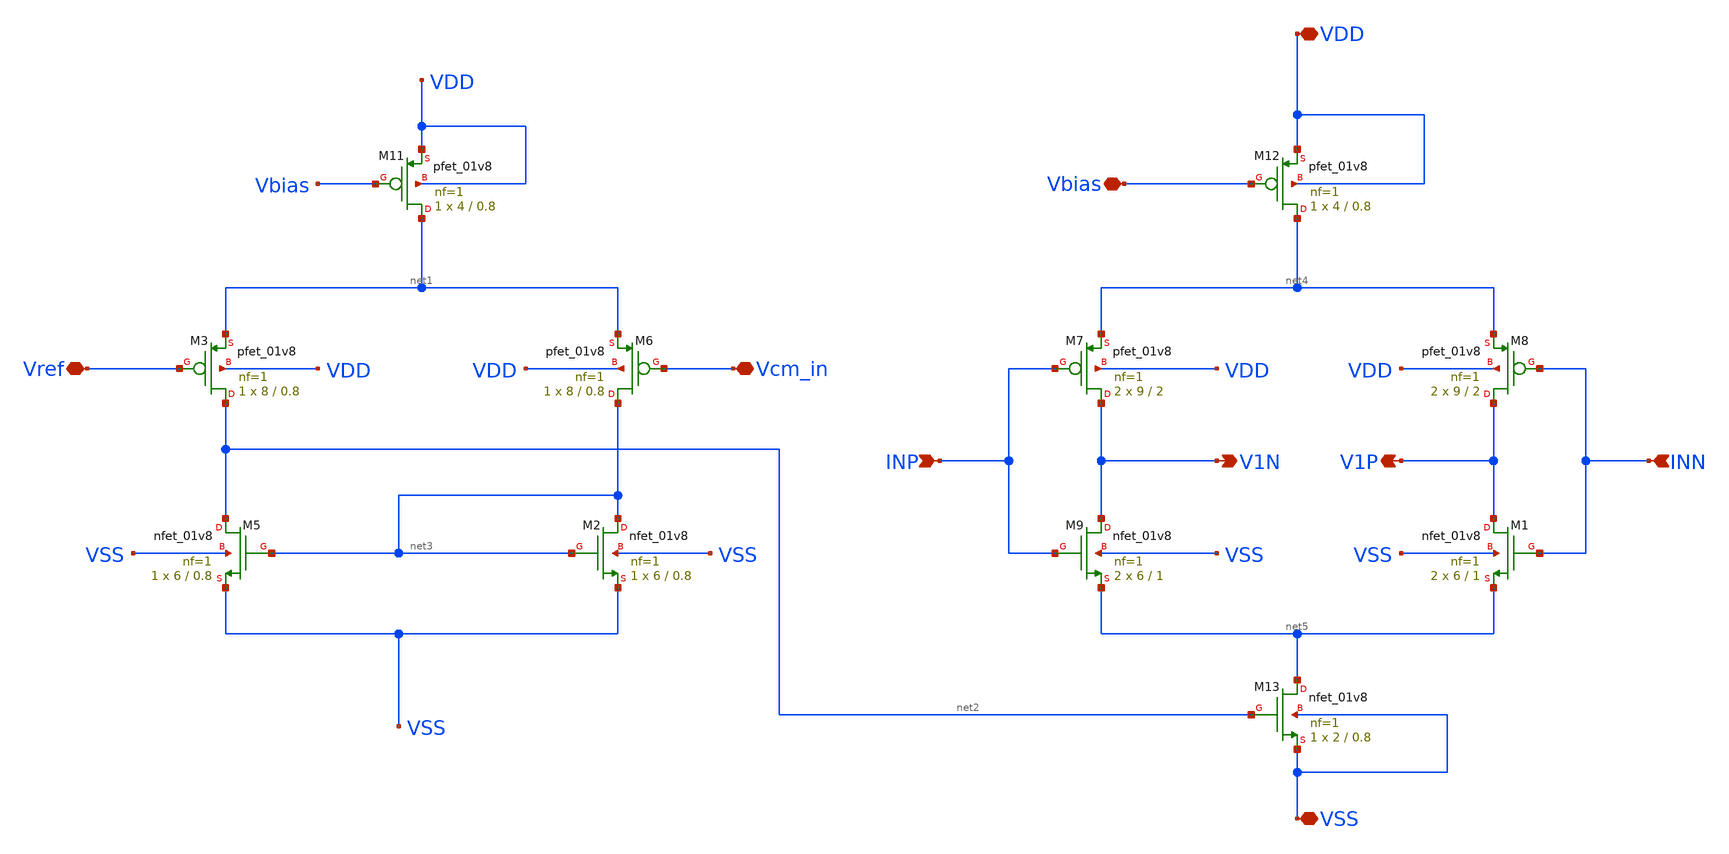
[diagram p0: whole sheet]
** sch_path: opamp_lna/low_noise_amp_simp.sch
**.subckt low_noise_amp_simp VDD VSS Vbias INP INN Vref Vcm_in V1N V1P
*.iopin VDD
*.iopin VSS
*.iopin Vbias
*.ipin INP
*.ipin INN
*.iopin Vref
*.iopin Vcm_in
*.opin V1N
*.opin V1P
XM3 net2 Vref net1 VDD sky130_fd_pr__pfet_01v8 L=0.8 W=8 nf=1 ad='int((nf+1)/2) * W/nf * 0.29' as='int((nf+2)/2) * W/nf * 0.29'
+ pd='2*int((nf+1)/2) * (W/nf + 0.29)' ps='2*int((nf+2)/2) * (W/nf + 0.29)' nrd='0.29 / W' nrs='0.29 / W'
+ sa=0 sb=0 sd=0 mult=1 m=1
XM11 net1 Vbias VDD VDD sky130_fd_pr__pfet_01v8 L=0.8 W=4 nf=1 ad='int((nf+1)/2) * W/nf * 0.29' as='int((nf+2)/2) * W/nf * 0.29'
+ pd='2*int((nf+1)/2) * (W/nf + 0.29)' ps='2*int((nf+2)/2) * (W/nf + 0.29)' nrd='0.29 / W' nrs='0.29 / W'
+ sa=0 sb=0 sd=0 mult=1 m=1
XM7 V1N INP net4 VDD sky130_fd_pr__pfet_01v8 L=2 W=9 nf=1 ad='int((nf+1)/2) * W/nf * 0.29' as='int((nf+2)/2) * W/nf * 0.29'
+ pd='2*int((nf+1)/2) * (W/nf + 0.29)' ps='2*int((nf+2)/2) * (W/nf + 0.29)' nrd='0.29 / W' nrs='0.29 / W'
+ sa=0 sb=0 sd=0 mult=2 m=2
XM8 V1P INN net4 VDD sky130_fd_pr__pfet_01v8 L=2 W=9 nf=1 ad='int((nf+1)/2) * W/nf * 0.29' as='int((nf+2)/2) * W/nf * 0.29'
+ pd='2*int((nf+1)/2) * (W/nf + 0.29)' ps='2*int((nf+2)/2) * (W/nf + 0.29)' nrd='0.29 / W' nrs='0.29 / W'
+ sa=0 sb=0 sd=0 mult=2 m=2
XM9 V1N INP net5 VSS sky130_fd_pr__nfet_01v8 L=1 W=6 nf=1 ad='int((nf+1)/2) * W/nf * 0.29' as='int((nf+2)/2) * W/nf * 0.29'
+ pd='2*int((nf+1)/2) * (W/nf + 0.29)' ps='2*int((nf+2)/2) * (W/nf + 0.29)' nrd='0.29 / W' nrs='0.29 / W'
+ sa=0 sb=0 sd=0 mult=2 m=2
XM12 net4 Vbias VDD VDD sky130_fd_pr__pfet_01v8 L=0.8 W=4 nf=1 ad='int((nf+1)/2) * W/nf * 0.29' as='int((nf+2)/2) * W/nf * 0.29'
+ pd='2*int((nf+1)/2) * (W/nf + 0.29)' ps='2*int((nf+2)/2) * (W/nf + 0.29)' nrd='0.29 / W' nrs='0.29 / W'
+ sa=0 sb=0 sd=0 mult=1 m=1
XM13 net5 net2 VSS VSS sky130_fd_pr__nfet_01v8 L=0.8 W=2 nf=1 ad='int((nf+1)/2) * W/nf * 0.29' as='int((nf+2)/2) * W/nf * 0.29'
+ pd='2*int((nf+1)/2) * (W/nf + 0.29)' ps='2*int((nf+2)/2) * (W/nf + 0.29)' nrd='0.29 / W' nrs='0.29 / W'
+ sa=0 sb=0 sd=0 mult=1 m=1
XM1 V1P INN net5 VSS sky130_fd_pr__nfet_01v8 L=1 W=6 nf=1 ad='int((nf+1)/2) * W/nf * 0.29' as='int((nf+2)/2) * W/nf * 0.29'
+ pd='2*int((nf+1)/2) * (W/nf + 0.29)' ps='2*int((nf+2)/2) * (W/nf + 0.29)' nrd='0.29 / W' nrs='0.29 / W'
+ sa=0 sb=0 sd=0 mult=2 m=2
XM2 net3 net3 VSS VSS sky130_fd_pr__nfet_01v8 L=0.8 W=6 nf=1 ad='int((nf+1)/2) * W/nf * 0.29' as='int((nf+2)/2) * W/nf * 0.29'
+ pd='2*int((nf+1)/2) * (W/nf + 0.29)' ps='2*int((nf+2)/2) * (W/nf + 0.29)' nrd='0.29 / W' nrs='0.29 / W'
+ sa=0 sb=0 sd=0 mult=1 m=1
XM5 net2 net3 VSS VSS sky130_fd_pr__nfet_01v8 L=0.8 W=6 nf=1 ad='int((nf+1)/2) * W/nf * 0.29' as='int((nf+2)/2) * W/nf * 0.29'
+ pd='2*int((nf+1)/2) * (W/nf + 0.29)' ps='2*int((nf+2)/2) * (W/nf + 0.29)' nrd='0.29 / W' nrs='0.29 / W'
+ sa=0 sb=0 sd=0 mult=1 m=1
XM6 net3 Vcm_in net1 VDD sky130_fd_pr__pfet_01v8 L=0.8 W=8 nf=1 ad='int((nf+1)/2) * W/nf * 0.29' as='int((nf+2)/2) * W/nf * 0.29'
+ pd='2*int((nf+1)/2) * (W/nf + 0.29)' ps='2*int((nf+2)/2) * (W/nf + 0.29)' nrd='0.29 / W' nrs='0.29 / W'
+ sa=0 sb=0 sd=0 mult=1 m=1
**.ends
.end
